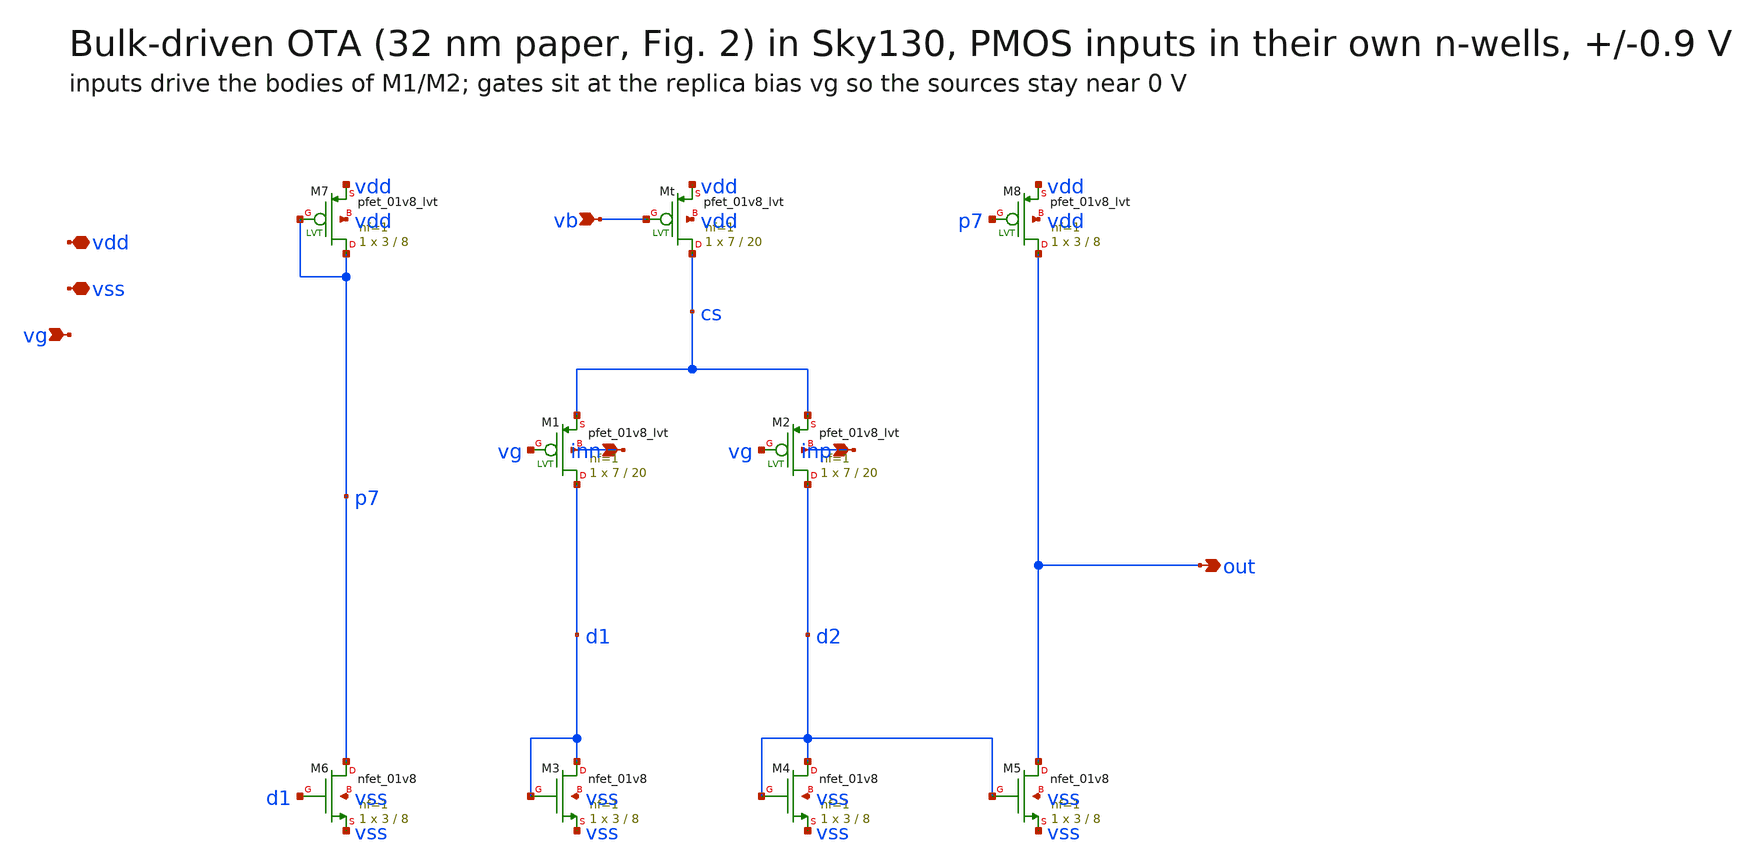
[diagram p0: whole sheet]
** sch_path: notch_ota_bulk_driven/schematics/ota_bd.sch
**.subckt ota_bd inn inp out vb vg vdd vss
*.ipin inn
*.ipin inp
*.opin out
*.ipin vb
*.ipin vg
*.iopin vdd
*.iopin vss
XM7 p7 p7 vdd vdd sky130_fd_pr__pfet_01v8_lvt L=8 W=3 nf=1 ad='int((nf+1)/2) * W/nf * 0.29' as='int((nf+2)/2) * W/nf * 0.29'
+ pd='2*int((nf+1)/2) * (W/nf + 0.29)' ps='2*int((nf+2)/2) * (W/nf + 0.29)' nrd='0.29 / W' nrs='0.29 / W'
+ sa=0 sb=0 sd=0 mult=1 m=1
XMt cs vb vdd vdd sky130_fd_pr__pfet_01v8_lvt L=20 W=7 nf=1 ad='int((nf+1)/2) * W/nf * 0.29' as='int((nf+2)/2) * W/nf * 0.29'
+ pd='2*int((nf+1)/2) * (W/nf + 0.29)' ps='2*int((nf+2)/2) * (W/nf + 0.29)' nrd='0.29 / W' nrs='0.29 / W'
+ sa=0 sb=0 sd=0 mult=1 m=1
XM8 out p7 vdd vdd sky130_fd_pr__pfet_01v8_lvt L=8 W=3 nf=1 ad='int((nf+1)/2) * W/nf * 0.29' as='int((nf+2)/2) * W/nf * 0.29'
+ pd='2*int((nf+1)/2) * (W/nf + 0.29)' ps='2*int((nf+2)/2) * (W/nf + 0.29)' nrd='0.29 / W' nrs='0.29 / W'
+ sa=0 sb=0 sd=0 mult=1 m=1
XM1 d1 vg cs inn sky130_fd_pr__pfet_01v8_lvt L=20 W=7 nf=1 ad='int((nf+1)/2) * W/nf * 0.29' as='int((nf+2)/2) * W/nf * 0.29'
+ pd='2*int((nf+1)/2) * (W/nf + 0.29)' ps='2*int((nf+2)/2) * (W/nf + 0.29)' nrd='0.29 / W' nrs='0.29 / W'
+ sa=0 sb=0 sd=0 mult=1 m=1
XM2 d2 vg cs inp sky130_fd_pr__pfet_01v8_lvt L=20 W=7 nf=1 ad='int((nf+1)/2) * W/nf * 0.29' as='int((nf+2)/2) * W/nf * 0.29'
+ pd='2*int((nf+1)/2) * (W/nf + 0.29)' ps='2*int((nf+2)/2) * (W/nf + 0.29)' nrd='0.29 / W' nrs='0.29 / W'
+ sa=0 sb=0 sd=0 mult=1 m=1
XM6 p7 d1 vss vss sky130_fd_pr__nfet_01v8 L=8 W=3 nf=1 ad='int((nf+1)/2) * W/nf * 0.29' as='int((nf+2)/2) * W/nf * 0.29'
+ pd='2*int((nf+1)/2) * (W/nf + 0.29)' ps='2*int((nf+2)/2) * (W/nf + 0.29)' nrd='0.29 / W' nrs='0.29 / W'
+ sa=0 sb=0 sd=0 mult=1 m=1
XM3 d1 d1 vss vss sky130_fd_pr__nfet_01v8 L=8 W=3 nf=1 ad='int((nf+1)/2) * W/nf * 0.29' as='int((nf+2)/2) * W/nf * 0.29'
+ pd='2*int((nf+1)/2) * (W/nf + 0.29)' ps='2*int((nf+2)/2) * (W/nf + 0.29)' nrd='0.29 / W' nrs='0.29 / W'
+ sa=0 sb=0 sd=0 mult=1 m=1
XM4 d2 d2 vss vss sky130_fd_pr__nfet_01v8 L=8 W=3 nf=1 ad='int((nf+1)/2) * W/nf * 0.29' as='int((nf+2)/2) * W/nf * 0.29'
+ pd='2*int((nf+1)/2) * (W/nf + 0.29)' ps='2*int((nf+2)/2) * (W/nf + 0.29)' nrd='0.29 / W' nrs='0.29 / W'
+ sa=0 sb=0 sd=0 mult=1 m=1
XM5 out d2 vss vss sky130_fd_pr__nfet_01v8 L=8 W=3 nf=1 ad='int((nf+1)/2) * W/nf * 0.29' as='int((nf+2)/2) * W/nf * 0.29'
+ pd='2*int((nf+1)/2) * (W/nf + 0.29)' ps='2*int((nf+2)/2) * (W/nf + 0.29)' nrd='0.29 / W' nrs='0.29 / W'
+ sa=0 sb=0 sd=0 mult=1 m=1
**.ends
.end
